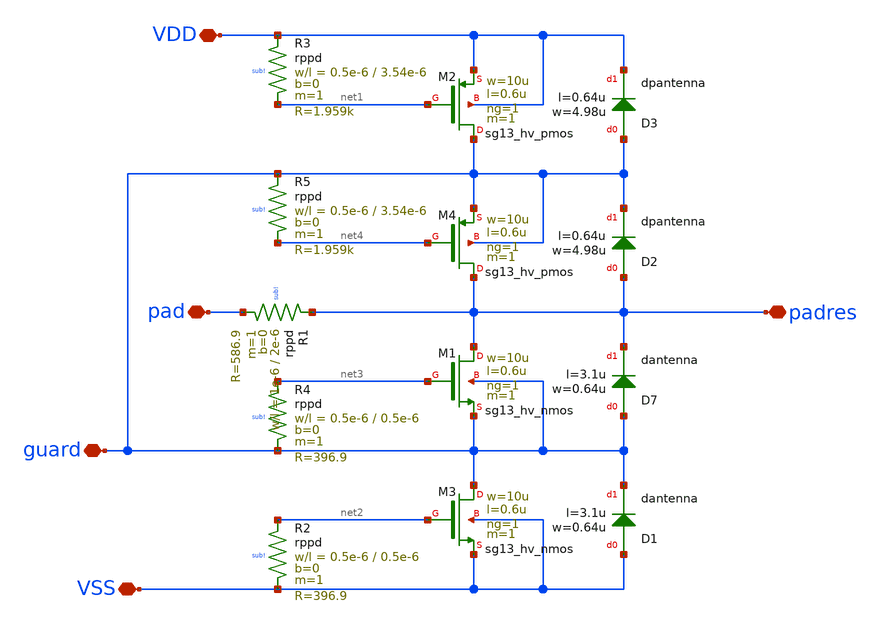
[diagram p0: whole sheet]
** sch_path: trident_test_structures/design_data/xschem/IOPadAnalogGuardLayer/secondary_protection_low_vt_guard_layer.sch
**.subckt secondary_protection_low_vt_guard_layer VSS VDD pad guard padres
*.iopin VSS
*.iopin VDD
*.iopin pad
*.iopin guard
*.iopin padres
XR1 padres pad sub! rppd w=1e-6 l=2e-6 m=1 b=0 mm_ok=1
XD7 guard padres dantenna l=3.1u w=0.64u
XD1 VSS guard dantenna l=3.1u w=0.64u
XD2 padres guard dpantenna l=0.64u w=4.98u
XD3 guard VDD dpantenna l=0.64u w=4.98u
XM2 guard net1 VDD VDD sg13_hv_pmos w=10u l=0.6u ng=1 m=1 mm_ok=1
XR3 VDD net1 sub! rppd w=0.5e-6 l=3.54e-6 m=1 b=0 mm_ok=1
XM3 guard net2 VSS VSS sg13_hv_nmos w=10u l=0.6u ng=1 m=1 mm_ok=1
XR2 net2 VSS sub! rppd w=0.5e-6 l=0.5e-6 m=1 b=0 mm_ok=1
XM1 padres net3 guard guard sg13_hv_nmos w=10u l=0.6u ng=1 m=1 mm_ok=1
XR4 net3 guard sub! rppd w=0.5e-6 l=0.5e-6 m=1 b=0 mm_ok=1
XM4 padres net4 guard guard sg13_hv_pmos w=10u l=0.6u ng=1 m=1 mm_ok=1
XR5 guard net4 sub! rppd w=0.5e-6 l=3.54e-6 m=1 b=0 mm_ok=1
**.ends
.end
